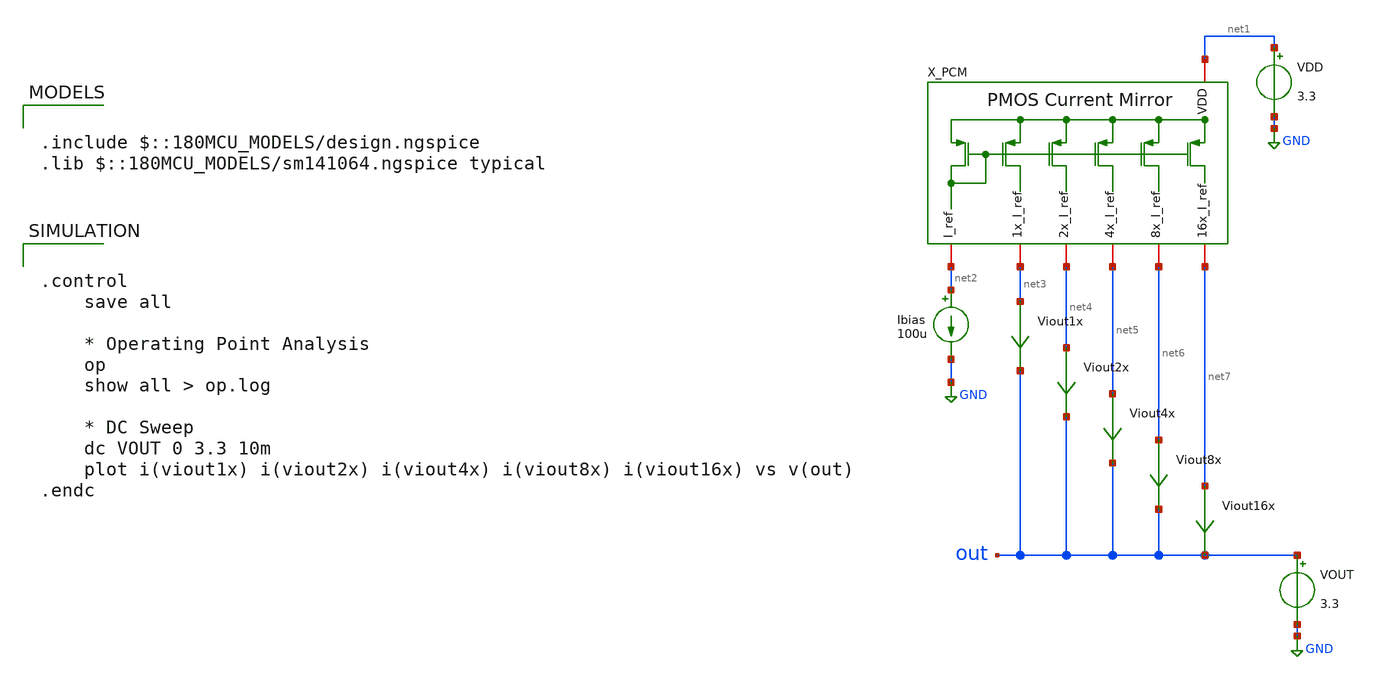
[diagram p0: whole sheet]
** sch_path: designs/libs/tb_current_mirror/tb_pmos_current_mirror.sch
**.subckt tb_pmos_current_mirror
X_PCM net1 net2 net3 net4 net5 net6 net7 pmos_current_mirror
VDD net1 GND 3.3
Viout1x net3 out 0
.save i(viout1x)
Ibias net2 GND 100u
Viout2x net4 out 0
.save i(viout2x)
Viout4x net5 out 0
.save i(viout4x)
Viout16x net7 out 0
.save i(viout16x)
Viout8x net6 out 0
.save i(viout8x)
VOUT out GND 3.3
**** begin user architecture code

.include $::180MCU_MODELS/design.ngspice
.lib $::180MCU_MODELS/sm141064.ngspice typical



.control
    save all

    * Operating Point Analysis
    op
    show all > op.log

    * DC Sweep
    dc VOUT 0 3.3 10m
    plot i(viout1x) i(viout2x) i(viout4x) i(viout8x) i(viout16x) vs v(out)
.endc


**** end user architecture code
**.ends

* expanding   symbol:  libs/core_current_mirror/pmos_current_mirror/pmos_current_mirror.sym # of
*+ pins=7
** sym_path: designs/libs/core_current_mirror/pmos_current_mirror/pmos_current_mirror.sym
** sch_path: designs/libs/core_current_mirror/pmos_current_mirror/pmos_current_mirror.sch
.subckt pmos_current_mirror VDD I_ref 1x_I_ref 2x_I_ref 4x_I_ref 8x_I_ref 16x_I_ref
*.iopin I_ref
*.iopin VDD
*.iopin 1x_I_ref
*.iopin 2x_I_ref
*.iopin 4x_I_ref
*.iopin 8x_I_ref
*.iopin 16x_I_ref
XIREF I_ref VDD I_ref VDD unit_pmos M=1
X1x 1x_I_ref VDD I_ref VDD unit_pmos M=1
X2x 2x_I_ref VDD I_ref VDD unit_pmos M=2
X4x 4x_I_ref VDD I_ref VDD unit_pmos M=4
X8x 8x_I_ref VDD I_ref VDD unit_pmos M=8
X16x 16x_I_ref VDD I_ref VDD unit_pmos M=16
.ends


* expanding   symbol:  libs/core_single_mos/unit_pmos/unit_pmos.sym # of pins=4
** sym_path: designs/libs/core_single_mos/unit_pmos/unit_pmos.sym
** sch_path: designs/libs/core_single_mos/unit_pmos/unit_pmos.sch
.subckt unit_pmos drain sub gate source
*.iopin drain
*.iopin source
*.iopin sub
*.iopin gate
**** begin user architecture code

.param M=1

**** end user architecture code
XM1 drain gate source sub pfet_03v3 L=0.5u W=48u nf=8 ad='int((nf+1)/2) * W/nf * 0.18u' as='int((nf+2)/2) * W/nf * 0.18u'
+ pd='2*int((nf+1)/2) * (W/nf + 0.18u)' ps='2*int((nf+2)/2) * (W/nf + 0.18u)' nrd='0.18u / W' nrs='0.18u / W'
+ sa=0 sb=0 sd=0 m={M}
.ends

.GLOBAL GND
.end
